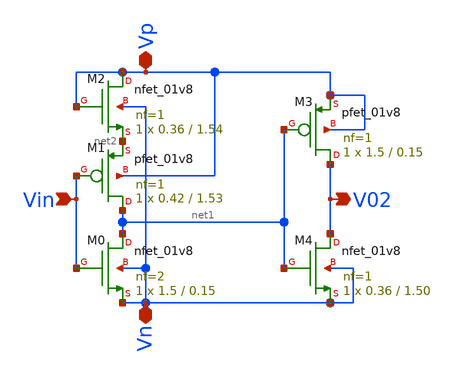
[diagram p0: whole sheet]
** sch_path: xschem/Vth_sch/Symbol/th02.sch
**.subckt th02 Vin V02 Vp Vn
*.ipin Vin
*.opin V02
*.iopin Vp
*.iopin Vn
XM3 V02 net1 Vp Vp sky130_fd_pr__pfet_01v8 L=0.15 W=1.5 nf=1 ad='int((nf+1)/2) * W/nf * 0.29' as='int((nf+2)/2) * W/nf * 0.29'
+ pd='2*int((nf+1)/2) * (W/nf + 0.29)' ps='2*int((nf+2)/2) * (W/nf + 0.29)' nrd='0.29 / W' nrs='0.29 / W'
+ sa=0 sb=0 sd=0 mult=1 m=1
XM4 V02 net1 Vn Vn sky130_fd_pr__nfet_01v8 L=1.50 W=0.36 nf=1 ad='int((nf+1)/2) * W/nf * 0.29' as='int((nf+2)/2) * W/nf * 0.29'
+ pd='2*int((nf+1)/2) * (W/nf + 0.29)' ps='2*int((nf+2)/2) * (W/nf + 0.29)' nrd='0.29 / W' nrs='0.29 / W'
+ sa=0 sb=0 sd=0 mult=1 m=1
XM1 net1 Vin net2 Vp sky130_fd_pr__pfet_01v8 L=1.53 W=0.42 nf=1 ad='int((nf+1)/2) * W/nf * 0.29' as='int((nf+2)/2) * W/nf * 0.29'
+ pd='2*int((nf+1)/2) * (W/nf + 0.29)' ps='2*int((nf+2)/2) * (W/nf + 0.29)' nrd='0.29 / W' nrs='0.29 / W'
+ sa=0 sb=0 sd=0 mult=1 m=1
XM0 net1 Vin Vn Vn sky130_fd_pr__nfet_01v8 L=0.15 W=1.5 nf=2 ad='int((nf+1)/2) * W/nf * 0.29' as='int((nf+2)/2) * W/nf * 0.29'
+ pd='2*int((nf+1)/2) * (W/nf + 0.29)' ps='2*int((nf+2)/2) * (W/nf + 0.29)' nrd='0.29 / W' nrs='0.29 / W'
+ sa=0 sb=0 sd=0 mult=1 m=1
XM2 Vp Vp net2 Vn sky130_fd_pr__nfet_01v8 L=1.54 W=0.36 nf=1 ad='int((nf+1)/2) * W/nf * 0.29' as='int((nf+2)/2) * W/nf * 0.29'
+ pd='2*int((nf+1)/2) * (W/nf + 0.29)' ps='2*int((nf+2)/2) * (W/nf + 0.29)' nrd='0.29 / W' nrs='0.29 / W'
+ sa=0 sb=0 sd=0 mult=1 m=1
**.ends
.end
